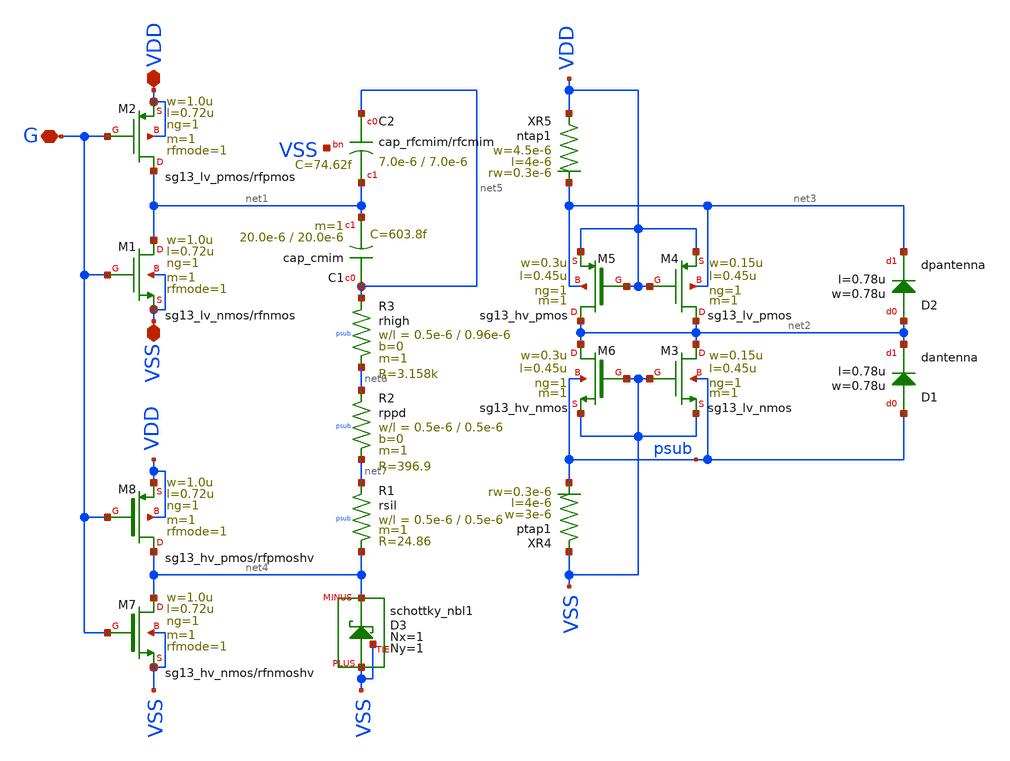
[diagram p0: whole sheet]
** sch_path: LVS-testbenches/schematic/sg13_combined_cmim_ontop.sch
**.subckt sg13_combined_cmim_ontop VDD VSS G
*.iopin VDD
*.iopin VSS
*.iopin G
XC1 net5 net1 cap_cmim w=20.0e-6 l=20.0e-6 m=1 mm_ok=1
XM1 net1 G VSS VSS sg13_lv_nmos w=1.0u l=0.72u ng=1 m=1 rfmode=1 mm_ok=1
XM2 net1 G VDD VDD sg13_lv_pmos w=1.0u l=0.72u ng=1 m=1 rfmode=1 mm_ok=1
XD1 psub net2 dantenna l=0.78u w=0.78u
XD2 net2 net3 dpantenna l=0.78u w=0.78u
XD3 VSS net4 VSS schottky_nbl1 Nx=1 Ny=1
XM3 net2 VSS VSS psub sg13_lv_nmos w=0.15u l=0.45u ng=1 m=1 mm_ok=1
XM4 net2 VDD VDD net3 sg13_lv_pmos w=0.15u l=0.45u ng=1 m=1 mm_ok=1
XM5 net2 VDD VDD net3 sg13_hv_pmos w=0.3u l=0.45u ng=1 m=1 mm_ok=1
XM6 net2 VSS VSS psub sg13_hv_nmos w=0.3u l=0.45u ng=1 m=1 mm_ok=1
XM7 net4 G VSS VSS sg13_hv_nmos w=1.0u l=0.72u ng=1 m=1 rfmode=1 mm_ok=1
XM8 net4 G VDD VDD sg13_hv_pmos w=1.0u l=0.72u ng=1 m=1 rfmode=1 mm_ok=1
XR1 net7 net4 psub rsil w=0.5e-6 l=0.5e-6 m=1 mm_ok=1
XR2 net6 net7 psub rppd w=0.5e-6 l=0.5e-6 m=1 b=0 mm_ok=1
XR3 net5 net6 psub rhigh w=0.5e-6 l=0.96e-6 m=1 b=0 mm_ok=1
XR4 VSS psub ptap1 R=17.81 w=3e-6 l=4e-6 rw=0.3e-6
XR5 VDD net3 ntap1 R=14.42 w=4.5e-6 l=4e-6 rw=0.3e-6
XC2 net5 net1 VSS cap_rfcmim w=7.0e-6 l=7.0e-6 wfeed=3.0e-6 m=1 mm_ok=1
**.ends
.end
